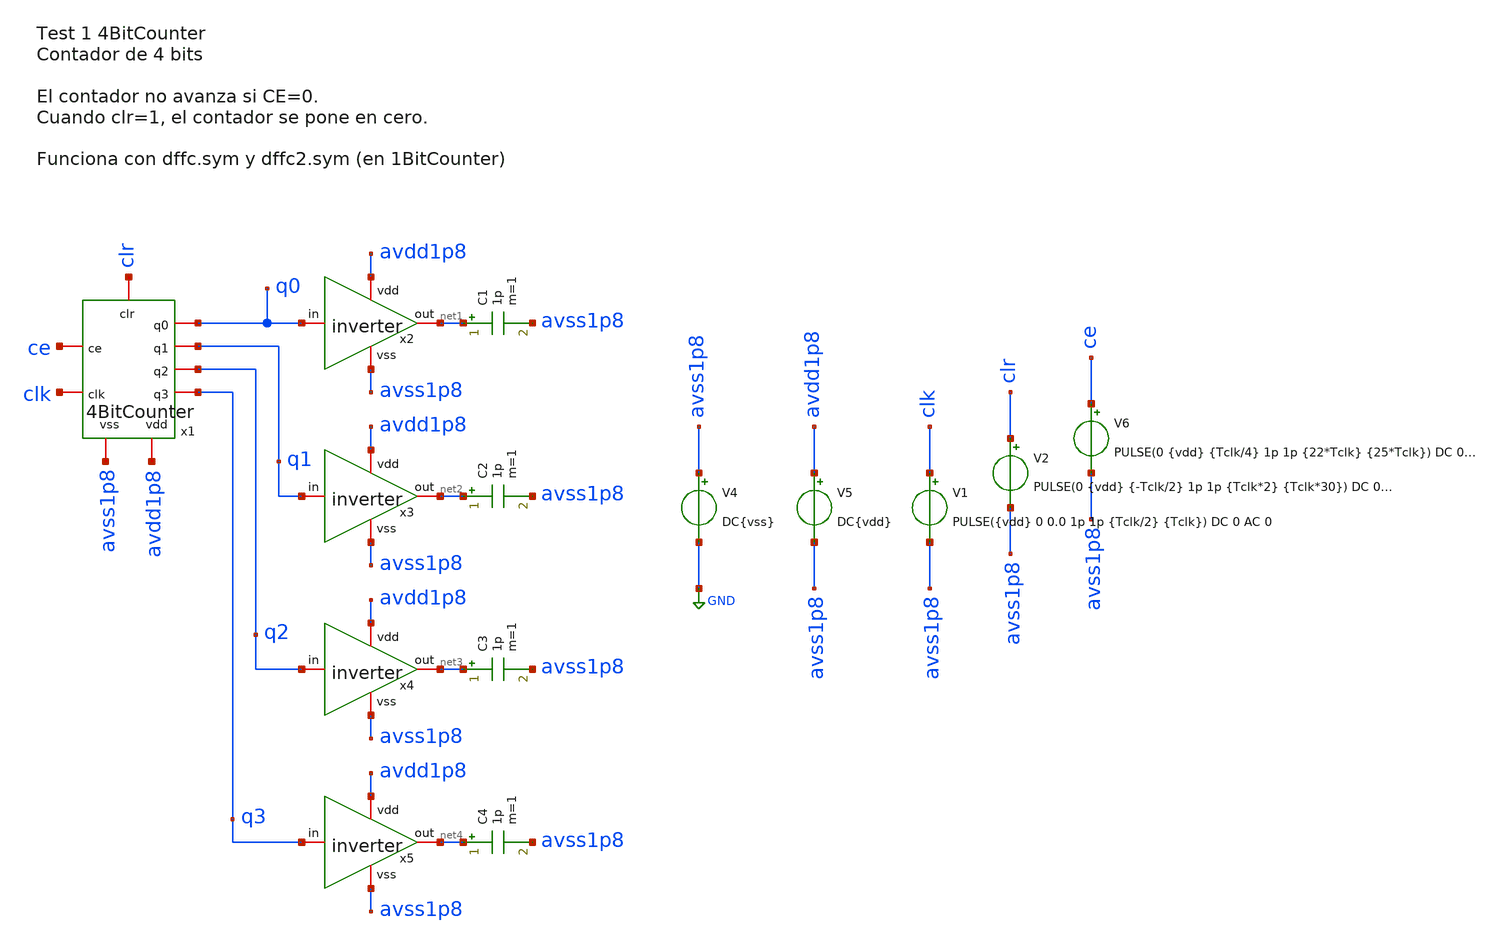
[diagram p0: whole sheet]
** sch_path: designs/sch/tests/test1_4BitCounter.sch
**.subckt test1_4BitCounter
x2 avdd1p8 net1 q0 avss1p8 inverter
V4 avss1p8 GND DC{vss}
V5 avdd1p8 avss1p8 DC{vdd}
V6 ce avss1p8 PULSE(0 {vdd} {Tclk/4} 1p 1p {22*Tclk} {25*Tclk}) DC 0 AC 0
C1 net1 avss1p8 1p m=1
V1 clk avss1p8 PULSE({vdd} 0 0.0 1p 1p {Tclk/2} {Tclk}) DC 0 AC 0
V2 clr avss1p8 PULSE(0 {vdd} {-Tclk/2} 1p 1p {Tclk*2} {Tclk*30}) DC 0 AC 0
x1 q2 q1 q0 q3 clr clk ce avdd1p8 avss1p8 4BitCounter
x3 avdd1p8 net2 q1 avss1p8 inverter
C2 net2 avss1p8 1p m=1
x4 avdd1p8 net3 q2 avss1p8 inverter
C3 net3 avss1p8 1p m=1
x5 avdd1p8 net4 q3 avss1p8 inverter
C4 net4 avss1p8 1p m=1
**** begin user architecture code


* Circuit Parameters
.param vdd = 1.8
.param vss = 0.0
.param Tclk = 15n
.options TEMP = 65.0

* Include Models
.lib /foss/pdks/sky130A/libs.tech/ngspice/sky130.lib.spice TT

* OP Parameters & Singals to save
.save all

* Simulations
.control
  tran 0.01u 1u
  setplot tran1
  plot clr ce+2 v(q0)+4 v(q1)+6 v(q2)+8 v(q3)+10 clk+12
reset
.endc

.end


**** end user architecture code
**.ends
.GLOBAL GND
.end
